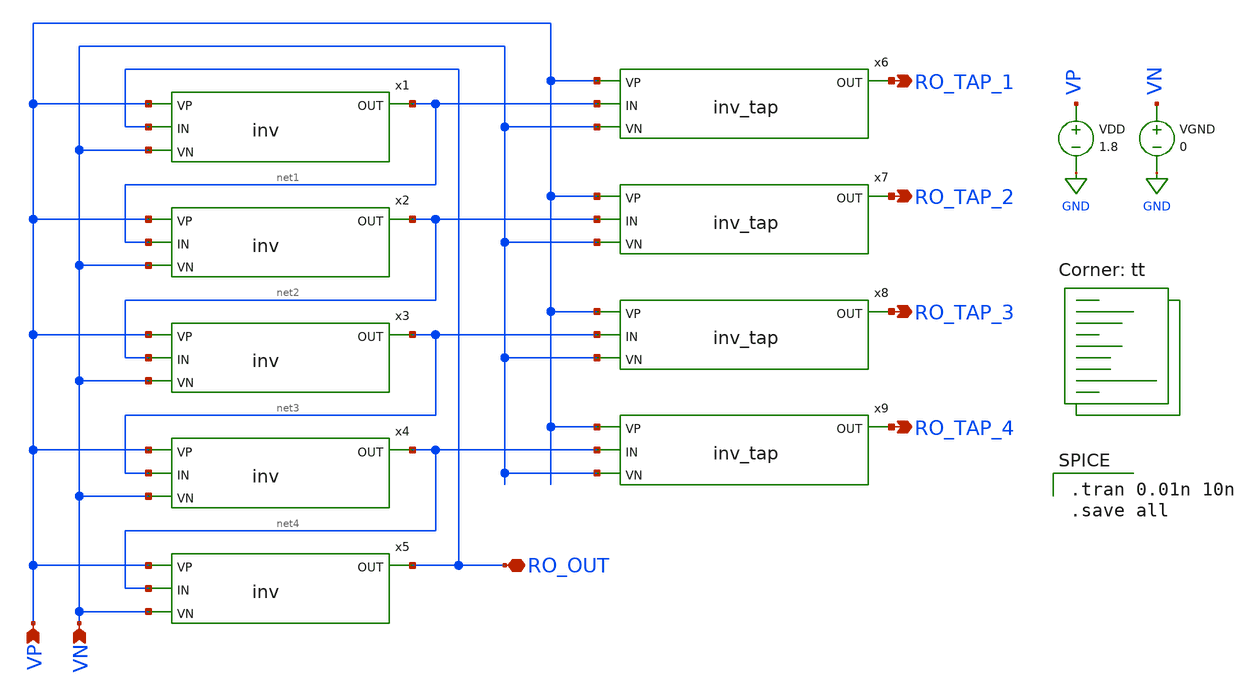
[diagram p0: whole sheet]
** sch_path: Mixed-Signal TRNG/xschem/ro.sch
**.subckt ro RO_OUT VP VN RO_TAP_1 RO_TAP_2 RO_TAP_3 RO_TAP_4
*.iopin RO_OUT
*.ipin VP
*.ipin VN
*.opin RO_TAP_1
*.opin RO_TAP_2
*.opin RO_TAP_3
*.opin RO_TAP_4
x1 VP RO_OUT net1 VN inv
x2 VP net1 net2 VN inv
x3 VP net2 net3 VN inv
x4 VP net3 net4 VN inv
x5 VP net4 RO_OUT VN inv
VDD VP GND 1.8
VGND VN GND 0
x6 VP net1 RO_TAP_1 VN inv_tap
x7 VP net2 RO_TAP_2 VN inv_tap
x8 VP net3 RO_TAP_3 VN inv_tap
x9 VP net4 RO_TAP_4 VN inv_tap
**** begin user architecture code

.tran 0.01n 10n
.save all

.lib $::SKYWATER_MODELS/sky130.lib.spice tt
**** end user architecture code
**.ends

* expanding   symbol:  /home/madvlsi/Desktop/Mixed-Signal TRNG/xschem/inv.sym # of pins=4
** sym_path: Mixed-Signal TRNG/xschem/inv.sym
** sch_path: Mixed-Signal TRNG/xschem/inv.sch
.subckt inv VP IN OUT VN
*.ipin IN
*.opin OUT
*.ipin VP
*.ipin VN
XM1 OUT IN VN VN sky130_fd_pr__nfet_01v8 L=0.15 W=2 nf=1 ad='int((nf+1)/2) * W/nf * 0.29' as='int((nf+2)/2) * W/nf * 0.29'
+ pd='2*int((nf+1)/2) * (W/nf + 0.29)' ps='2*int((nf+2)/2) * (W/nf + 0.29)' nrd='0.29 / W' nrs='0.29 / W'
+ sa=0 sb=0 sd=0 mult=1 m=1
XM2 OUT IN VP VP sky130_fd_pr__pfet_01v8 L=0.15 W=4 nf=1 ad='int((nf+1)/2) * W/nf * 0.29' as='int((nf+2)/2) * W/nf * 0.29'
+ pd='2*int((nf+1)/2) * (W/nf + 0.29)' ps='2*int((nf+2)/2) * (W/nf + 0.29)' nrd='0.29 / W' nrs='0.29 / W'
+ sa=0 sb=0 sd=0 mult=1 m=1
.ends


* expanding   symbol:  /home/madvlsi/Desktop/Mixed-Signal TRNG/xschem/inv_tap.sym # of pins=4
** sym_path: Mixed-Signal TRNG/xschem/inv_tap.sym
** sch_path: Mixed-Signal TRNG/xschem/inv_tap.sch
.subckt inv_tap VP IN OUT VN
*.ipin IN
*.opin OUT
*.ipin VP
*.ipin VN
XM1 OUT IN VN VN sky130_fd_pr__nfet_01v8 L=0.15 W=0.6 nf=1 ad='int((nf+1)/2) * W/nf * 0.29' as='int((nf+2)/2) * W/nf * 0.29'
+ pd='2*int((nf+1)/2) * (W/nf + 0.29)' ps='2*int((nf+2)/2) * (W/nf + 0.29)' nrd='0.29 / W' nrs='0.29 / W'
+ sa=0 sb=0 sd=0 mult=1 m=1
XM2 OUT IN VP VP sky130_fd_pr__pfet_01v8 L=0.15 W=1.2 nf=1 ad='int((nf+1)/2) * W/nf * 0.29' as='int((nf+2)/2) * W/nf * 0.29'
+ pd='2*int((nf+1)/2) * (W/nf + 0.29)' ps='2*int((nf+2)/2) * (W/nf + 0.29)' nrd='0.29 / W' nrs='0.29 / W'
+ sa=0 sb=0 sd=0 mult=1 m=1
.ends

.GLOBAL GND
.end
